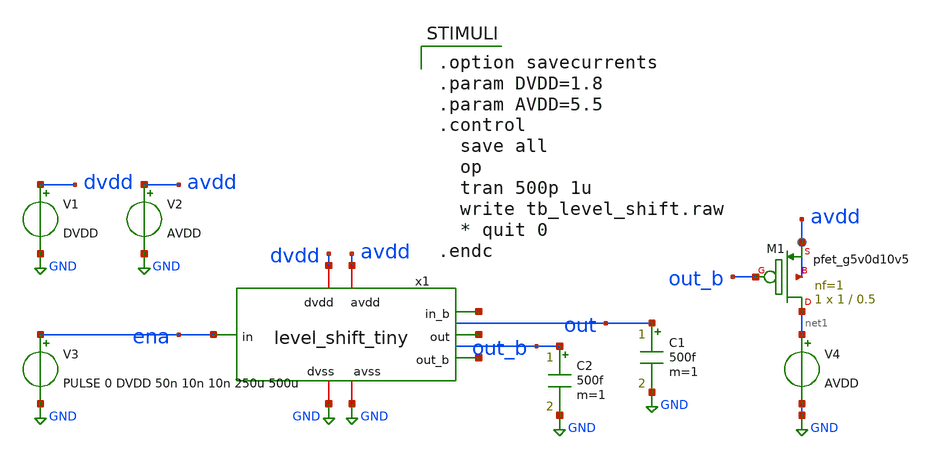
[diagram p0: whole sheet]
** sch_path: xschem/tb_level_shift.sch
* xschem/level_shift_tiny.sch:
* Copyright 2024 Brady Etz
* Licensed under the Apache License, Version 2.0 (the "License");

.lib $::SKYWATER_MODELS/sky130.lib.spice tt
*.include $::SKYWATER_STDCELLS/sky130_fd_sc_hd.spice

**.subckt tb_level_shift
V1 dvdd GND DVDD
V2 avdd GND AVDD
C1 out GND 500f m=1
C2 out_b GND 500f m=1
V3 ena GND PULSE 0 DVDD 50n 10n 10n 250u 500u
XM1 net1 out_b avdd avdd sky130_fd_pr__pfet_g5v0d10v5 L=0.5 W=1 nf=1 ad='int((nf+1)/2) * W/nf * 0.29'
+ as='int((nf+2)/2) * W/nf * 0.29' pd='2*int((nf+1)/2) * (W/nf + 0.29)' ps='2*int((nf+2)/2) * (W/nf + 0.29)'
+ nrd='0.29 / W' nrs='0.29 / W' sa=0 sb=0 sd=0 mult=1 m=1
V4 net1 GND AVDD
x1 avdd dvdd net2 net3 ena GND GND net4 level_shift_tiny
**** begin user architecture code

.option savecurrents
.param DVDD=1.8
.param AVDD=5.5
.control
  save all
  op
  tran 500p 1u
  write tb_level_shift.raw
  * quit 0
.endc

**** end user architecture code
**.ends

* expanding   symbol:  level_shift_tiny.sym # of pins=8
** sym_path: xschem/level_shift_tiny.sym
** sch_path: xschem/level_shift_tiny.sch
.subckt level_shift_tiny avdd dvdd out out_b in dvss avss in_b
*.ipin in
*.iopin avdd
*.iopin avss
*.iopin dvss
*.iopin dvdd
*.opin out
*.opin out_b
*.opin in_b
XM4 out in_b avss avss sky130_fd_pr__nfet_g5v0d10v5 L=0.5 W=6 nf=2 ad='int((nf+1)/2) * W/nf * 0.29' as='int((nf+2)/2) * W/nf * 0.29'
+ pd='2*int((nf+1)/2) * (W/nf + 0.29)' ps='2*int((nf+2)/2) * (W/nf + 0.29)' nrd='0.29 / W' nrs='0.29 / W'
+ sa=0 sb=0 sd=0 mult=1 m=1
XM3 out_b in avss avss sky130_fd_pr__nfet_g5v0d10v5 L=0.5 W=6 nf=2 ad='int((nf+1)/2) * W/nf * 0.29' as='int((nf+2)/2) * W/nf * 0.29'
+ pd='2*int((nf+1)/2) * (W/nf + 0.29)' ps='2*int((nf+2)/2) * (W/nf + 0.29)' nrd='0.29 / W' nrs='0.29 / W'
+ sa=0 sb=0 sd=0 mult=1 m=1
XM5 out_b out avdd avdd sky130_fd_pr__pfet_g5v0d10v5 L=4 W=1 nf=1 ad='int((nf+1)/2) * W/nf * 0.29' as='int((nf+2)/2) * W/nf * 0.29'
+ pd='2*int((nf+1)/2) * (W/nf + 0.29)' ps='2*int((nf+2)/2) * (W/nf + 0.29)' nrd='0.29 / W' nrs='0.29 / W'
+ sa=0 sb=0 sd=0 mult=1 m=1
XM6 out out_b avdd avdd sky130_fd_pr__pfet_g5v0d10v5 L=4 W=1 nf=1 ad='int((nf+1)/2) * W/nf * 0.29' as='int((nf+2)/2) * W/nf * 0.29'
+ pd='2*int((nf+1)/2) * (W/nf + 0.29)' ps='2*int((nf+2)/2) * (W/nf + 0.29)' nrd='0.29 / W' nrs='0.29 / W'
+ sa=0 sb=0 sd=0 mult=1 m=1
XM2 in_b in dvdd dvdd sky130_fd_pr__pfet_01v8 L=0.15 W=1 nf=1 ad='int((nf+1)/2) * W/nf * 0.29' as='int((nf+2)/2) * W/nf * 0.29'
+ pd='2*int((nf+1)/2) * (W/nf + 0.29)' ps='2*int((nf+2)/2) * (W/nf + 0.29)' nrd='0.29 / W' nrs='0.29 / W'
+ sa=0 sb=0 sd=0 mult=1 m=1
XM1 in_b in dvss dvss sky130_fd_pr__nfet_01v8 L=0.15 W=1 nf=1 ad='int((nf+1)/2) * W/nf * 0.29' as='int((nf+2)/2) * W/nf * 0.29'
+ pd='2*int((nf+1)/2) * (W/nf + 0.29)' ps='2*int((nf+2)/2) * (W/nf + 0.29)' nrd='0.29 / W' nrs='0.29 / W'
+ sa=0 sb=0 sd=0 mult=1 m=1
.ends

.GLOBAL GND
.end
